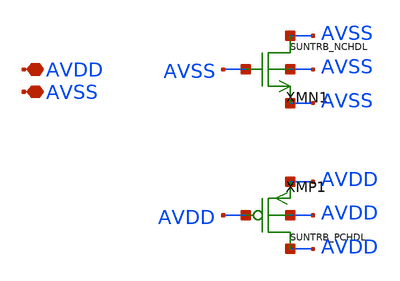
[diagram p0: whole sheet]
** sch_path: design/SUN_TRB_SKY130NM/SUNTRB_TAPCELLB_CV.sch
**.subckt SUNTRB_TAPCELLB_CV AVDD AVSS
*.iopin AVDD
*.iopin AVSS
XMN1 AVSS AVSS AVSS AVSS SUNTRB_NCHDL xoffset=0 yoffset=0 angle=0
XMP1 AVDD AVDD AVDD AVDD SUNTRB_PCHDL xoffset=0 yoffset=0 angle=0 M=1
**.ends
.end
